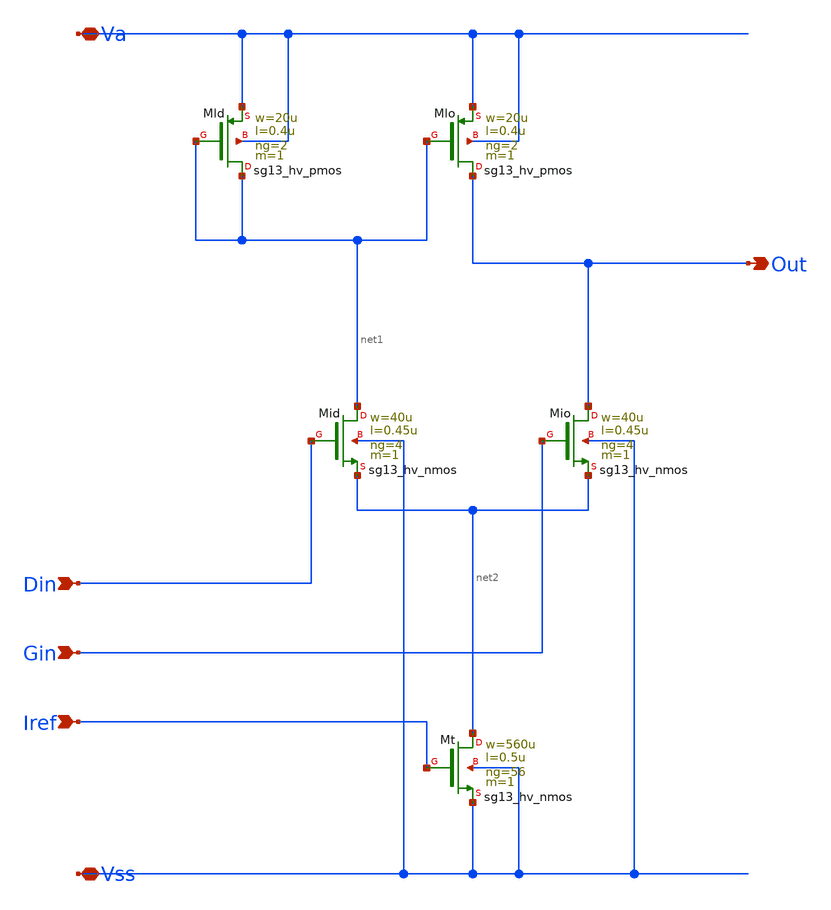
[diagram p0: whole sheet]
** sch_path: macros/lvds_tx/schematic/xschem/predriver_comp.sch
**.subckt predriver_comp Va Vss Out Din Gin Iref
*.iopin Va
*.iopin Vss
*.opin Out
*.ipin Din
*.ipin Gin
*.ipin Iref
XMld net1 net1 Va Va sg13_hv_pmos w=20u l=0.4u ng=2 m=1 mm_ok=1
XMlo Out net1 Va Va sg13_hv_pmos w=20u l=0.4u ng=2 m=1 mm_ok=1
XMid net1 Din net2 Vss sg13_hv_nmos w=40u l=0.45u ng=4 m=1 mm_ok=1
XMio Out Gin net2 Vss sg13_hv_nmos w=40u l=0.45u ng=4 m=1 mm_ok=1
XMt net2 Iref Vss Vss sg13_hv_nmos w=560u l=0.5u ng=56 m=1 mm_ok=1
**.ends
.end
